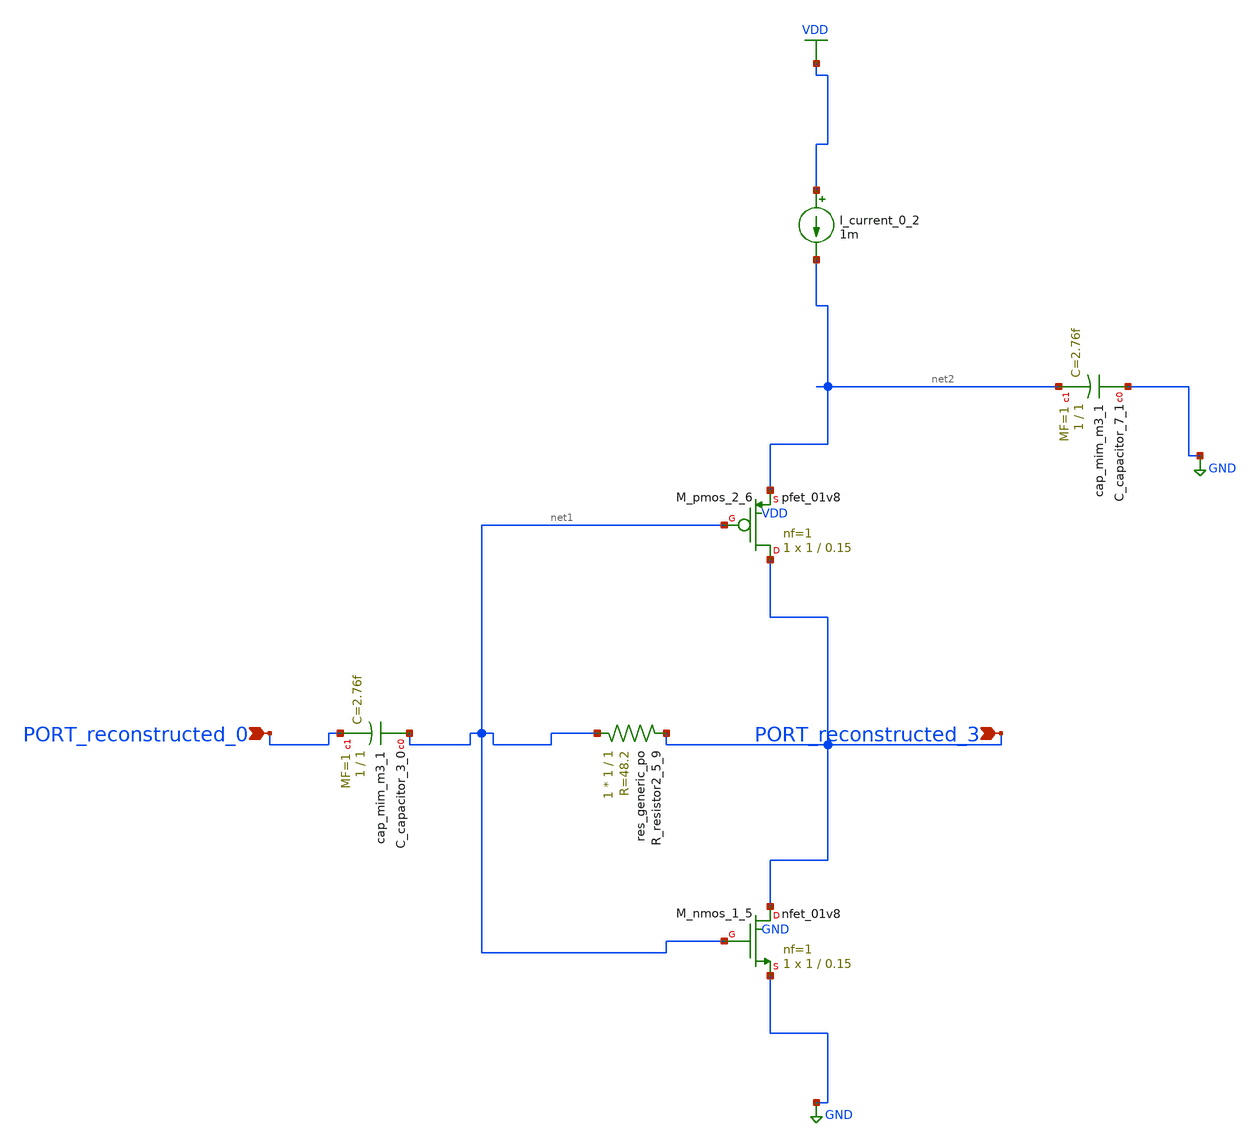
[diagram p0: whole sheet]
** sch_path: schematics/AMSNet/311.sch
**.subckt 311 PORT_reconstructed_0 PORT_reconstructed_3
*.ipin PORT_reconstructed_0
*.ipin PORT_reconstructed_3
XC_capacitor_3_0 net1 PORT_reconstructed_0 sky130_fd_pr__cap_mim_m3_1 W=1 L=1 MF=1 m=1
XC_capacitor_7_1 GND net2 sky130_fd_pr__cap_mim_m3_1 W=1 L=1 MF=1 m=1
I_current_0_2 VDD net2 1m
XM_nmos_1_5 PORT_reconstructed_3 net1 GND GND sky130_fd_pr__nfet_01v8 L=0.15 W=1 nf=1 ad='int((1 + 1)/2) * 1 / 1 * 0.29'
+ as='int((1 + 2)/2) * 1 / 1 * 0.29' pd='2*int((1 + 1)/2) * (1 / 1 + 0.29)' ps='2*int((1 + 2)/2) * (1 / 1 + 0.29)'
+ nrd='0.29 / 1 ' nrs='0.29 / 1 ' sa=0 sb=0 sd=0 mult=1 m=1
XM_pmos_2_6 PORT_reconstructed_3 net1 net2 VDD sky130_fd_pr__pfet_01v8 L=0.15 W=1 nf=1 ad='int((1 + 1)/2) * 1 / 1 * 0.29'
+ as='int((1 + 2)/2) * 1 / 1 * 0.29' pd='2*int((1 + 1)/2) * (1 / 1 + 0.29)' ps='2*int((1 + 2)/2) * (1 / 1 + 0.29)'
+ nrd='0.29 / 1 ' nrs='0.29 / 1 ' sa=0 sb=0 sd=0 mult=1 m=1
XR_resistor2_5_9 net1 PORT_reconstructed_3 sky130_fd_pr__res_generic_po W=1 L=1 m=1
**.ends
.GLOBAL GND
.GLOBAL VDD
.end
